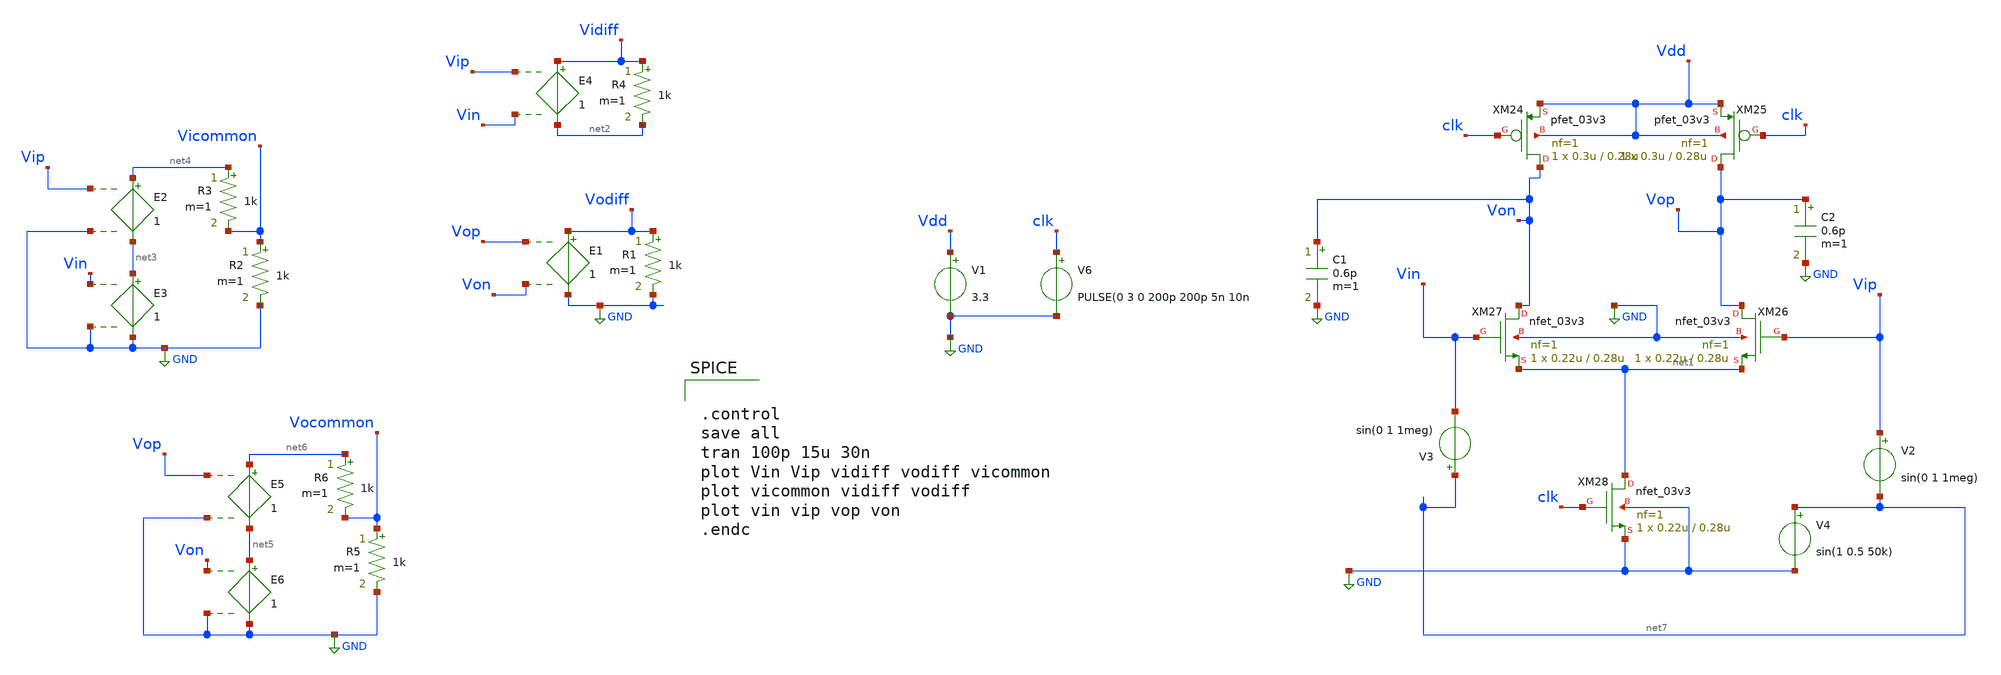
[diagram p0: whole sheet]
** sch_path: preamp/strongarm_cap.sch
**.subckt strongarm_cap
XM26 Vop Vip net1 GND nfet_03v3 L=0.28u W=0.22u nf=1 ad='int((nf+1)/2) * W/nf * 0.18u' as='int((nf+2)/2) * W/nf * 0.18u'
+ pd='2*int((nf+1)/2) * (W/nf + 0.18u)' ps='2*int((nf+2)/2) * (W/nf + 0.18u)' nrd='0.18u / W' nrs='0.18u / W'
+ sa=0 sb=0 sd=0 m=1
XM27 Von Vin net1 GND nfet_03v3 L=0.28u W=0.22u nf=1 ad='int((nf+1)/2) * W/nf * 0.18u' as='int((nf+2)/2) * W/nf * 0.18u'
+ pd='2*int((nf+1)/2) * (W/nf + 0.18u)' ps='2*int((nf+2)/2) * (W/nf + 0.18u)' nrd='0.18u / W' nrs='0.18u / W'
+ sa=0 sb=0 sd=0 m=1
R4 Vidiff net2 1k m=1
E4 Vidiff net2 Vip Vin 1
XM28 net1 clk GND GND nfet_03v3 L=0.28u W=0.22u nf=1 ad='int((nf+1)/2) * W/nf * 0.18u' as='int((nf+2)/2) * W/nf * 0.18u'
+ pd='2*int((nf+1)/2) * (W/nf + 0.18u)' ps='2*int((nf+2)/2) * (W/nf + 0.18u)' nrd='0.18u / W' nrs='0.18u / W'
+ sa=0 sb=0 sd=0 m=1
XM24 Von clk Vdd Vdd pfet_03v3 L=0.28u W=0.3u nf=1 ad='int((nf+1)/2) * W/nf * 0.18u' as='int((nf+2)/2) * W/nf * 0.18u'
+ pd='2*int((nf+1)/2) * (W/nf + 0.18u)' ps='2*int((nf+2)/2) * (W/nf + 0.18u)' nrd='0.18u / W' nrs='0.18u / W'
+ sa=0 sb=0 sd=0 m=1
XM25 Vop clk Vdd Vdd pfet_03v3 L=0.28u W=0.3u nf=1 ad='int((nf+1)/2) * W/nf * 0.18u' as='int((nf+2)/2) * W/nf * 0.18u'
+ pd='2*int((nf+1)/2) * (W/nf + 0.18u)' ps='2*int((nf+2)/2) * (W/nf + 0.18u)' nrd='0.18u / W' nrs='0.18u / W'
+ sa=0 sb=0 sd=0 m=1
R1 Vodiff GND 1k m=1
E1 Vodiff GND Vop Von 1
V6 clk GND PULSE(0 3 0 200p 200p 5n 10n
V2 Vip net7 sin(0 1 1meg)
E2 net4 net3 Vip GND 1
E3 net3 GND Vin GND 1
R2 Vicommon GND 1k m=1
R3 net4 Vicommon 1k m=1
E5 net6 net5 Vop GND 1
E6 net5 GND Von GND 1
R5 Vocommon GND 1k m=1
R6 net6 Vocommon 1k m=1
V1 Vdd GND 3.3
V4 net7 GND sin(1 0.5 50k)
V3 net7 Vin sin(0 1 1meg)
C1 Von GND 0.6p m=1
C2 Vop GND 0.6p m=1
**** begin user architecture code

.include /foss/pdks/gf180mcuC/libs.tech/ngspice/design.ngspice
.lib /foss/pdks/gf180mcuC/libs.tech/ngspice/sm141064.ngspice typical



.control
save all
tran 100p 15u 30n
plot Vin Vip vidiff vodiff vicommon
plot vicommon vidiff vodiff
plot vin vip vop von
.endc

**** end user architecture code
**.ends
.GLOBAL GND
.end
